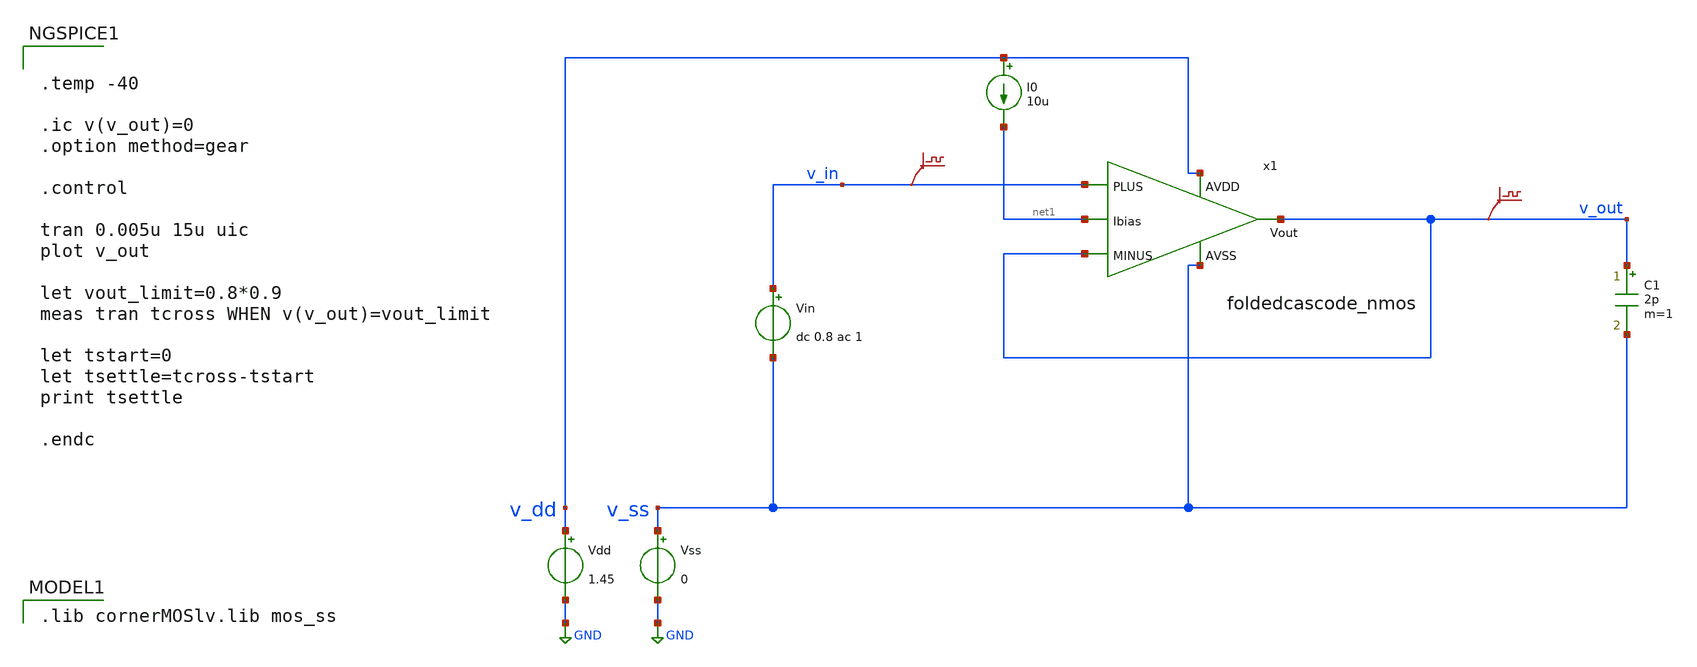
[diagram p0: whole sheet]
** sch_path: Designs/otas/tb_foldedcascode_nmos_tran.sch
* (c) 2025 Thesis_HP, Apache-2.0 license
**.subckt tb_foldedcascode_nmos_tran
Vdd v_dd GND 1.45
Vss v_ss GND 0
C1 v_out v_ss 2p m=1
Vin v_in v_ss dc 0.8 ac 1
I0 v_dd net1 10u
.save v(v_in)
.save v(v_out)
x1 v_dd v_in v_out v_out net1 v_ss foldedcascode_nmos
**** begin user architecture code
 .lib cornerMOSlv.lib mos_ss



.temp -40

.ic v(v_out)=0
.option method=gear

.control

tran 0.005u 15u uic
plot v_out

let vout_limit=0.8*0.9
meas tran tcross WHEN v(v_out)=vout_limit

let tstart=0
let tsettle=tcross-tstart
print tsettle

.endc


**** end user architecture code
**.ends

* expanding   symbol:  foldedcascode_nmos.sym # of pins=6
** sym_path: Designs/otas/foldedcascode_nmos.sym
** sch_path: Designs/otas/foldedcascode_nmos.sch
.subckt foldedcascode_nmos AVDD PLUS MINUS Vout Ibias AVSS
*.ipin PLUS
*.ipin MINUS
*.opin Vout
*.ipin AVDD
*.ipin AVSS
*.ipin Ibias
XM6 net5 PLUS net1 AVSS sg13_lv_nmos w=5u l=1u ng=1 m=1 mm_ok=1
XM8 net1 Ibias AVSS AVSS sg13_lv_nmos w=25u l=5u ng=3 m=1 mm_ok=1
XM21 net3 net4 AVSS AVSS sg13_lv_nmos w=1u l=0.5u ng=1 m=1 mm_ok=1
XM22 net2 net4 AVSS AVSS sg13_lv_nmos w=1u l=0.5u ng=1 m=1 mm_ok=1
XM7 net6 MINUS net1 AVSS sg13_lv_nmos w=5u l=1u ng=1 m=1 mm_ok=1
XM23 net4 net9 net2 AVSS sg13_lv_nmos w=1.5u l=0.5u ng=1 m=1 mm_ok=1
XM24 Vout net9 net3 AVSS sg13_lv_nmos w=1.5u l=0.5u ng=1 m=1 mm_ok=1
XM25 net4 net8 net5 AVDD sg13_lv_pmos w=6u l=0.5u ng=1 m=1 mm_ok=1
XM26 net5 net7 AVDD AVDD sg13_lv_pmos w=6u l=0.5u ng=1 m=1 mm_ok=1
XM27 Vout net8 net6 AVDD sg13_lv_pmos w=6u l=0.5u ng=1 m=1 mm_ok=1
XM28 net6 net7 AVDD AVDD sg13_lv_pmos w=6u l=0.5u ng=1 m=1 mm_ok=1
XM1 Ibias Ibias AVSS AVSS sg13_lv_nmos w=18u l=5u ng=2 m=1 mm_ok=1
XM2 net8 net8 net7 AVDD sg13_lv_pmos w=6u l=0.5u ng=2 m=1 mm_ok=1
XM3 net7 net7 AVDD AVDD sg13_lv_pmos w=6u l=0.5u ng=2 m=1 mm_ok=1
XM4 net9 net7 AVDD AVDD sg13_lv_pmos w=6u l=0.5u ng=2 m=1 mm_ok=1
XM5 net9 net9 AVSS AVSS sg13_lv_nmos w=1.5u l=0.5u ng=1 m=1 mm_ok=1
XM9 net8 Ibias AVSS AVSS sg13_lv_nmos w=25u l=5u ng=3 m=1 mm_ok=1
.ends

.GLOBAL GND
.end
